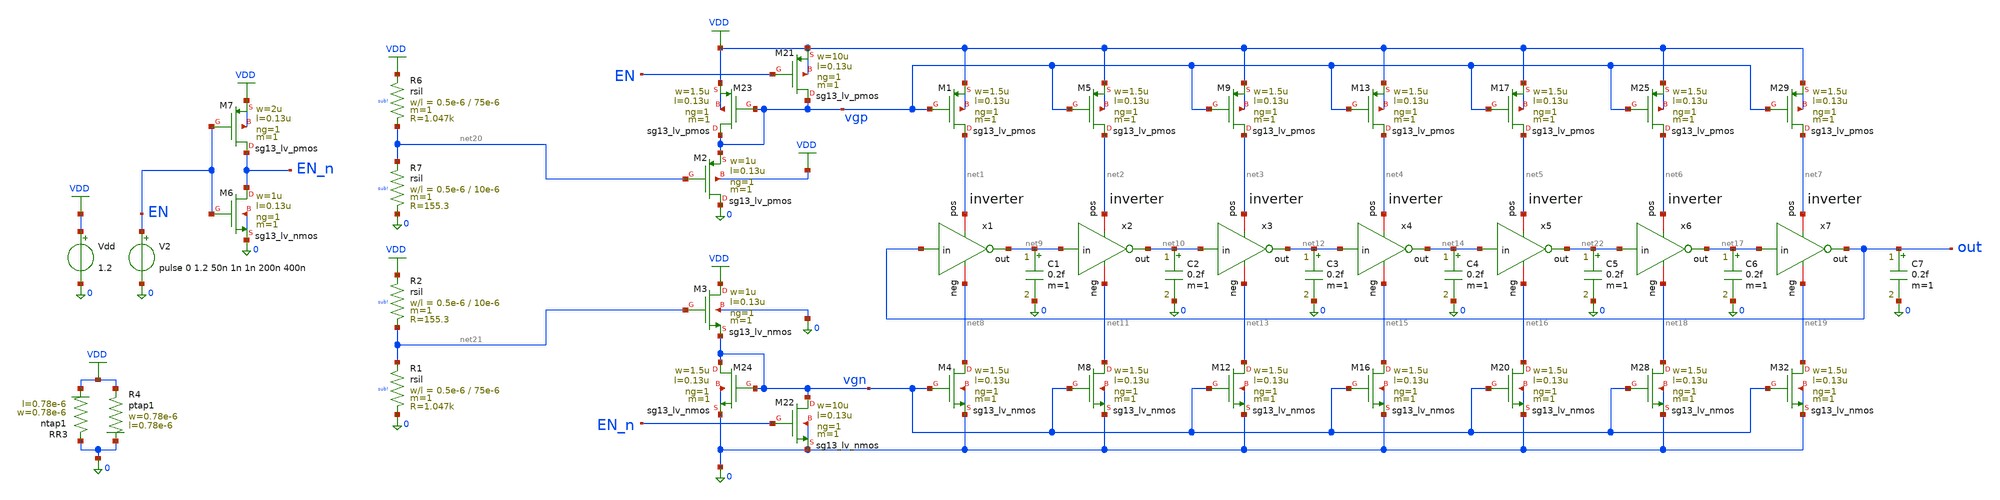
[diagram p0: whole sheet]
** sch_path: analog/temp-sens-core/testbenches/temp-sens-core_en-behavior.sch
**.subckt temp-sens-core_en-behavior
XM1 net1 vgp VDD VDD sg13_lv_pmos w=1.5u l=0.13u ng=1 m=1 mm_ok=1
XM21 vgp EN VDD VDD sg13_lv_pmos w=10u l=0.13u ng=1 m=1 mm_ok=1
XM22 vgn EN_n 0 0 sg13_lv_nmos w=10u l=0.13u ng=1 m=1 mm_ok=1
XM23 vgp vgp VDD VDD sg13_lv_pmos w=1.5u l=0.13u ng=1 m=1 mm_ok=1
XM24 vgn vgn 0 0 sg13_lv_nmos w=1.5u l=0.13u ng=1 m=1 mm_ok=1
Vdd VDD 0 1.2
XR3 0 VDD ntap1 R=262.8 w=0.78e-6 l=0.78e-6
XR4 VDD 0 ptap1 R=262.8 w=0.78e-6 l=0.78e-6
XM4 net8 vgn 0 0 sg13_lv_nmos w=1.5u l=0.13u ng=1 m=1 mm_ok=1
XM5 net2 vgp VDD VDD sg13_lv_pmos w=1.5u l=0.13u ng=1 m=1 mm_ok=1
XM8 net11 vgn 0 0 sg13_lv_nmos w=1.5u l=0.13u ng=1 m=1 mm_ok=1
XM9 net3 vgp VDD VDD sg13_lv_pmos w=1.5u l=0.13u ng=1 m=1 mm_ok=1
XM12 net13 vgn 0 0 sg13_lv_nmos w=1.5u l=0.13u ng=1 m=1 mm_ok=1
XM13 net4 vgp VDD VDD sg13_lv_pmos w=1.5u l=0.13u ng=1 m=1 mm_ok=1
XM16 net15 vgn 0 0 sg13_lv_nmos w=1.5u l=0.13u ng=1 m=1 mm_ok=1
XM17 net5 vgp VDD VDD sg13_lv_pmos w=1.5u l=0.13u ng=1 m=1 mm_ok=1
XM20 net16 vgn 0 0 sg13_lv_nmos w=1.5u l=0.13u ng=1 m=1 mm_ok=1
XM25 net6 vgp VDD VDD sg13_lv_pmos w=1.5u l=0.13u ng=1 m=1 mm_ok=1
XM28 net18 vgn 0 0 sg13_lv_nmos w=1.5u l=0.13u ng=1 m=1 mm_ok=1
XM29 net7 vgp VDD VDD sg13_lv_pmos w=1.5u l=0.13u ng=1 m=1 mm_ok=1
XM32 net19 vgn 0 0 sg13_lv_nmos w=1.5u l=0.13u ng=1 m=1 mm_ok=1
x1 net1 out net9 net8 inverter
x2 net2 net9 net10 net11 inverter
x3 net3 net10 net12 net13 inverter
x4 net4 net12 net14 net15 inverter
x5 net5 net14 net22 net16 inverter
x6 net6 net22 net17 net18 inverter
x7 net7 net17 out net19 inverter
XM2 0 net20 vgp VDD sg13_lv_pmos w=1u l=0.13u ng=1 m=1 mm_ok=1
XM3 VDD net21 vgn 0 sg13_lv_nmos w=1u l=0.13u ng=1 m=1 mm_ok=1
XR6 VDD net20 sub! rsil w=0.5e-6 l=75e-6 m=1 mm_ok=1
XR7 net20 0 sub! rsil w=0.5e-6 l=10e-6 m=1 mm_ok=1
XR1 net21 0 sub! rsil w=0.5e-6 l=75e-6 m=1 mm_ok=1
XR2 VDD net21 sub! rsil w=0.5e-6 l=10e-6 m=1 mm_ok=1
C1 net9 0 0.2f m=1
C2 net10 0 0.2f m=1
C3 net12 0 0.2f m=1
C4 net14 0 0.2f m=1
C5 net22 0 0.2f m=1
C6 net17 0 0.2f m=1
C7 out 0 0.2f m=1
XM6 EN_n EN 0 0 sg13_lv_nmos w=1u l=0.13u ng=1 m=1 mm_ok=1
XM7 EN_n EN VDD VDD sg13_lv_pmos w=2u l=0.13u ng=1 m=1 mm_ok=1
V2 EN 0 pulse 0 1.2 50n 1n 1n 200n 400n
**** begin user architecture code



.lib cornerMOSlv.lib mos_tt
.lib cornerMOShv.lib mos_tt
.lib cornerRES.lib res_typ
.lib cornerDIO.lib dio_tt






* ngspice commands
.option rshunt=1e12
.option klu
.control

tran 0.1n 1u

meas tran tperiod   TRIG v(out) VAL=0.9 RISE=2 TD=100n   TARG v(out) VAL=0.9 RISE=3 TD=100n

let f = 1/tperiod

write temp-sens-core_en-behavior.raw time out en en_n vgp vgn
.endc






.include /foss/pdks/ihp-sg13cmos5l/libs.ref/sg13cmos5l_stdcell/spice/sg13cmos5l_stdcell.spice



**** end user architecture code
**.ends

* expanding   symbol:  analog/inverter/inverter.sym # of pins=4
** sym_path: analog/inverter/inverter.sym
** sch_path: analog/inverter/inverter.sch
.subckt inverter pos in out neg
*.ipin in
*.iopin pos
*.iopin neg
*.opin out
XM1 out in neg neg sg13_lv_nmos w=2.0u l=0.45u ng=1 m=1 mm_ok=1
XM2 pos in out pos sg13_lv_pmos w=1.0u l=0.45u ng=1 m=1 mm_ok=1
.ends

.GLOBAL VDD
.end
